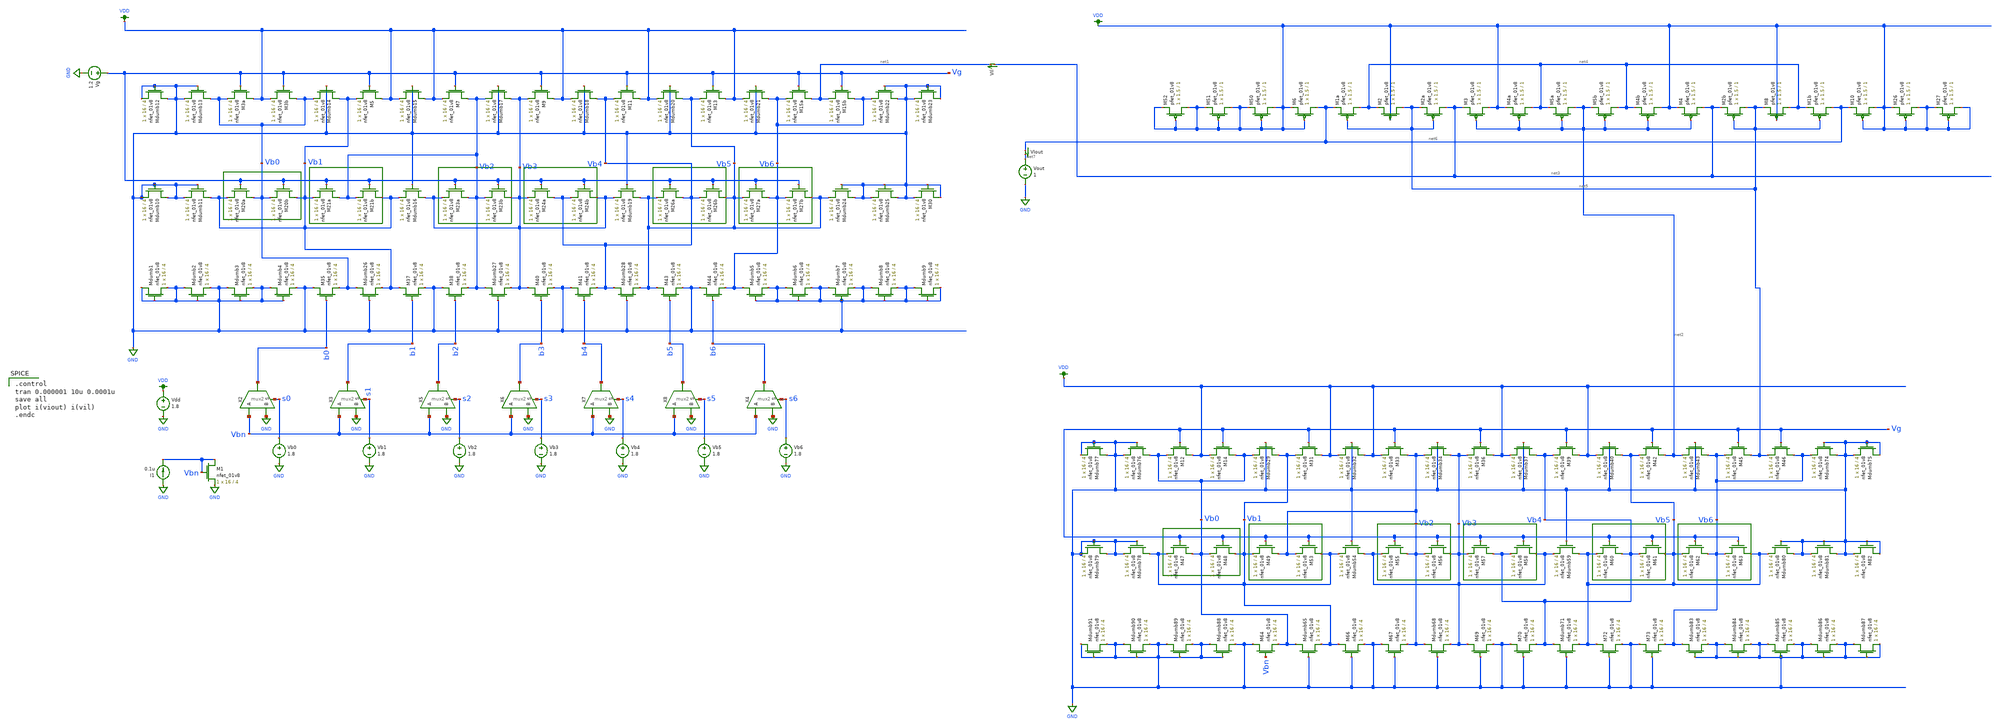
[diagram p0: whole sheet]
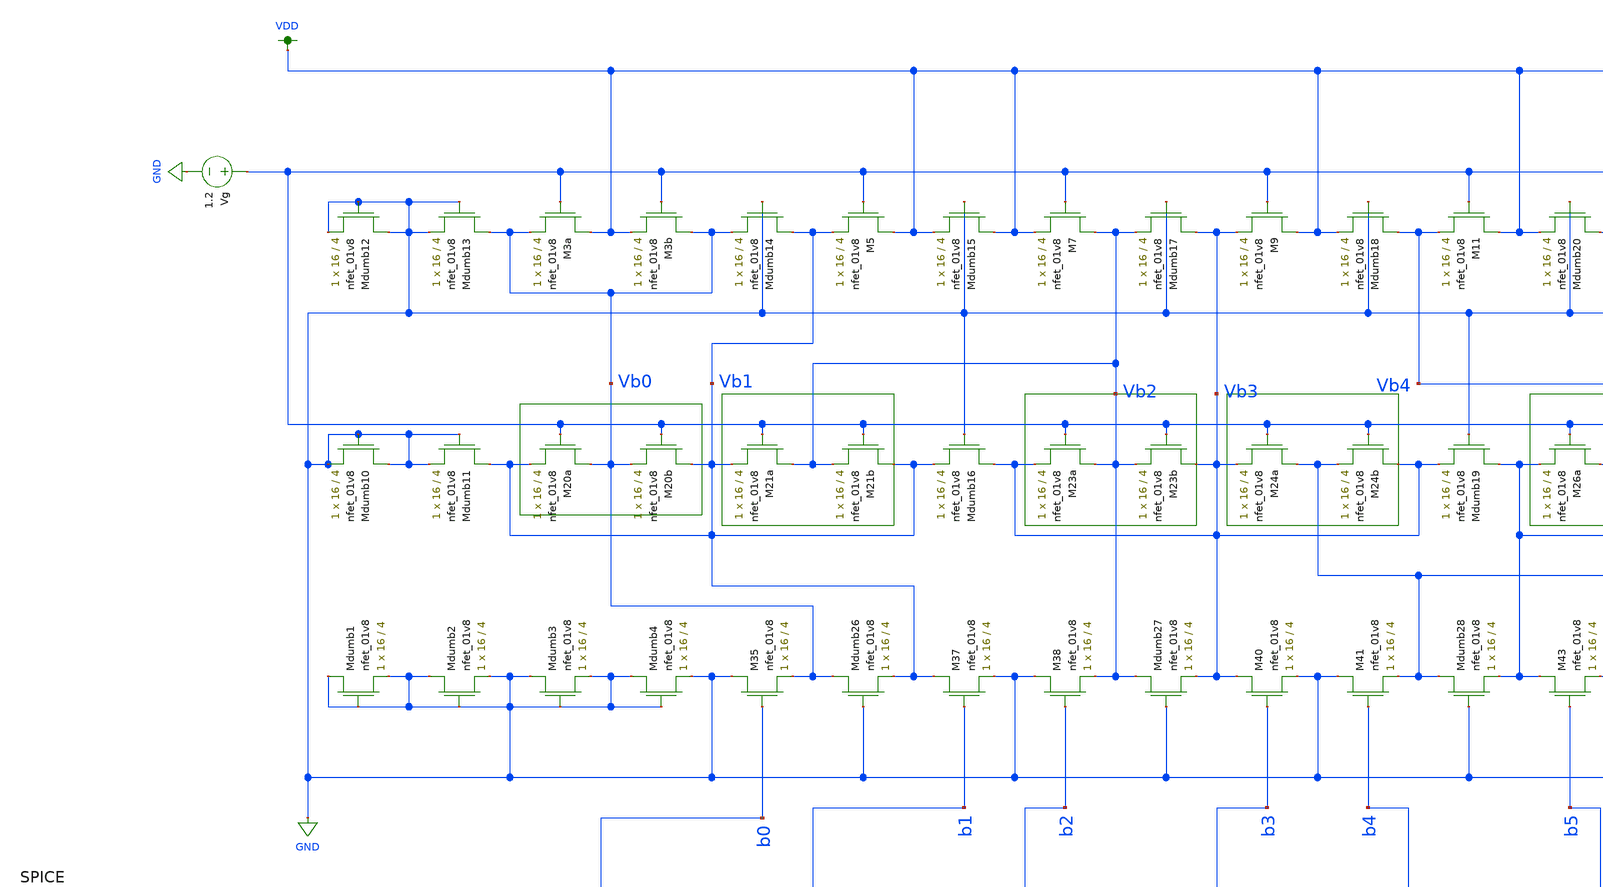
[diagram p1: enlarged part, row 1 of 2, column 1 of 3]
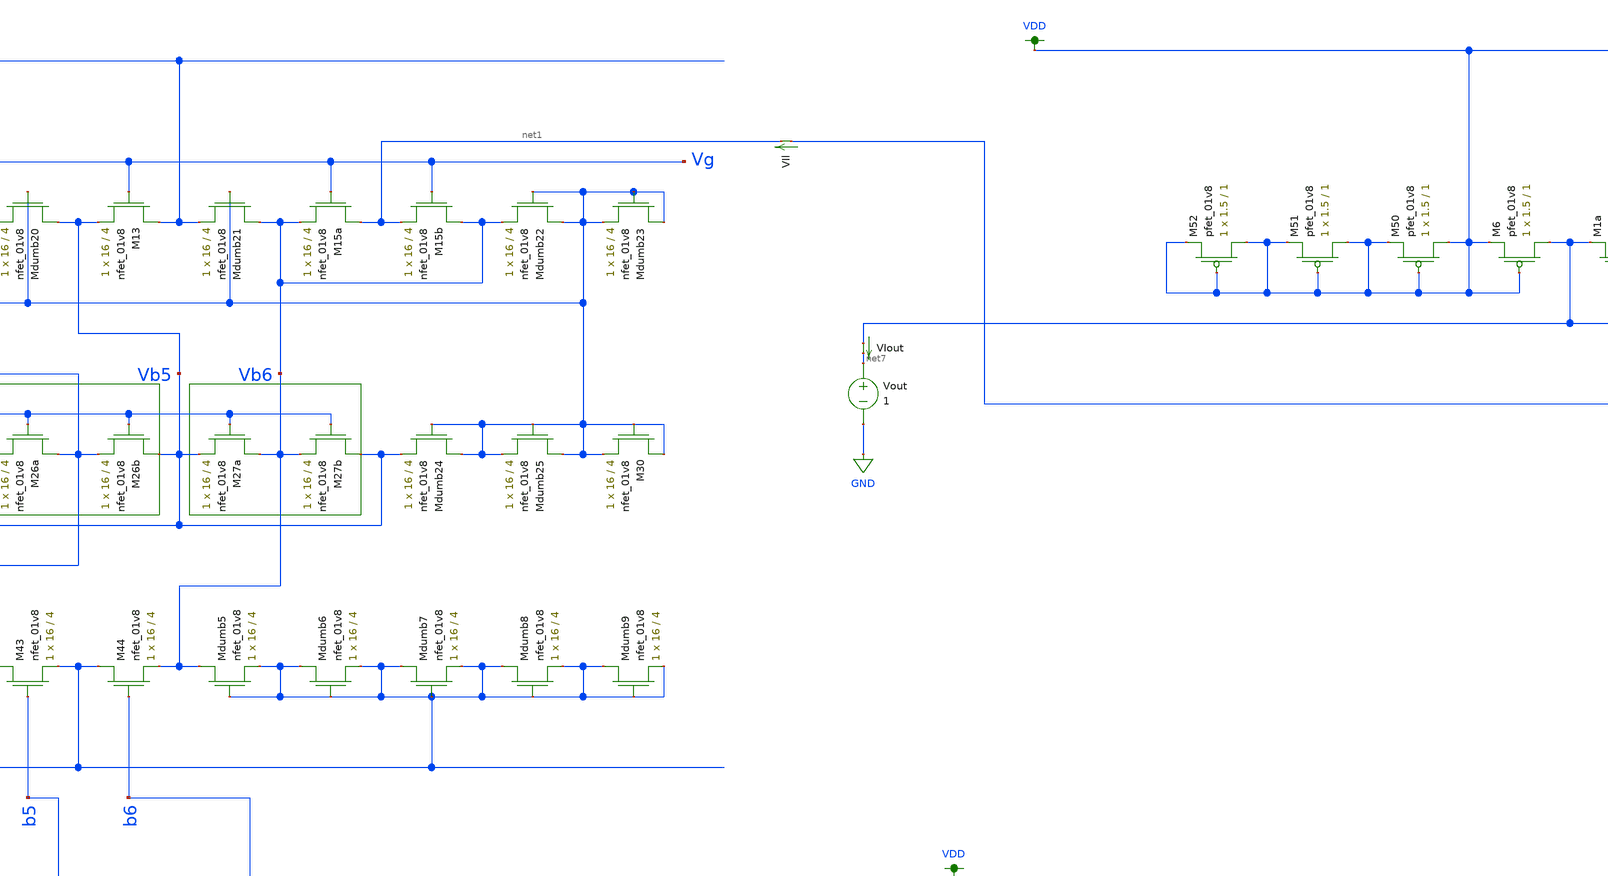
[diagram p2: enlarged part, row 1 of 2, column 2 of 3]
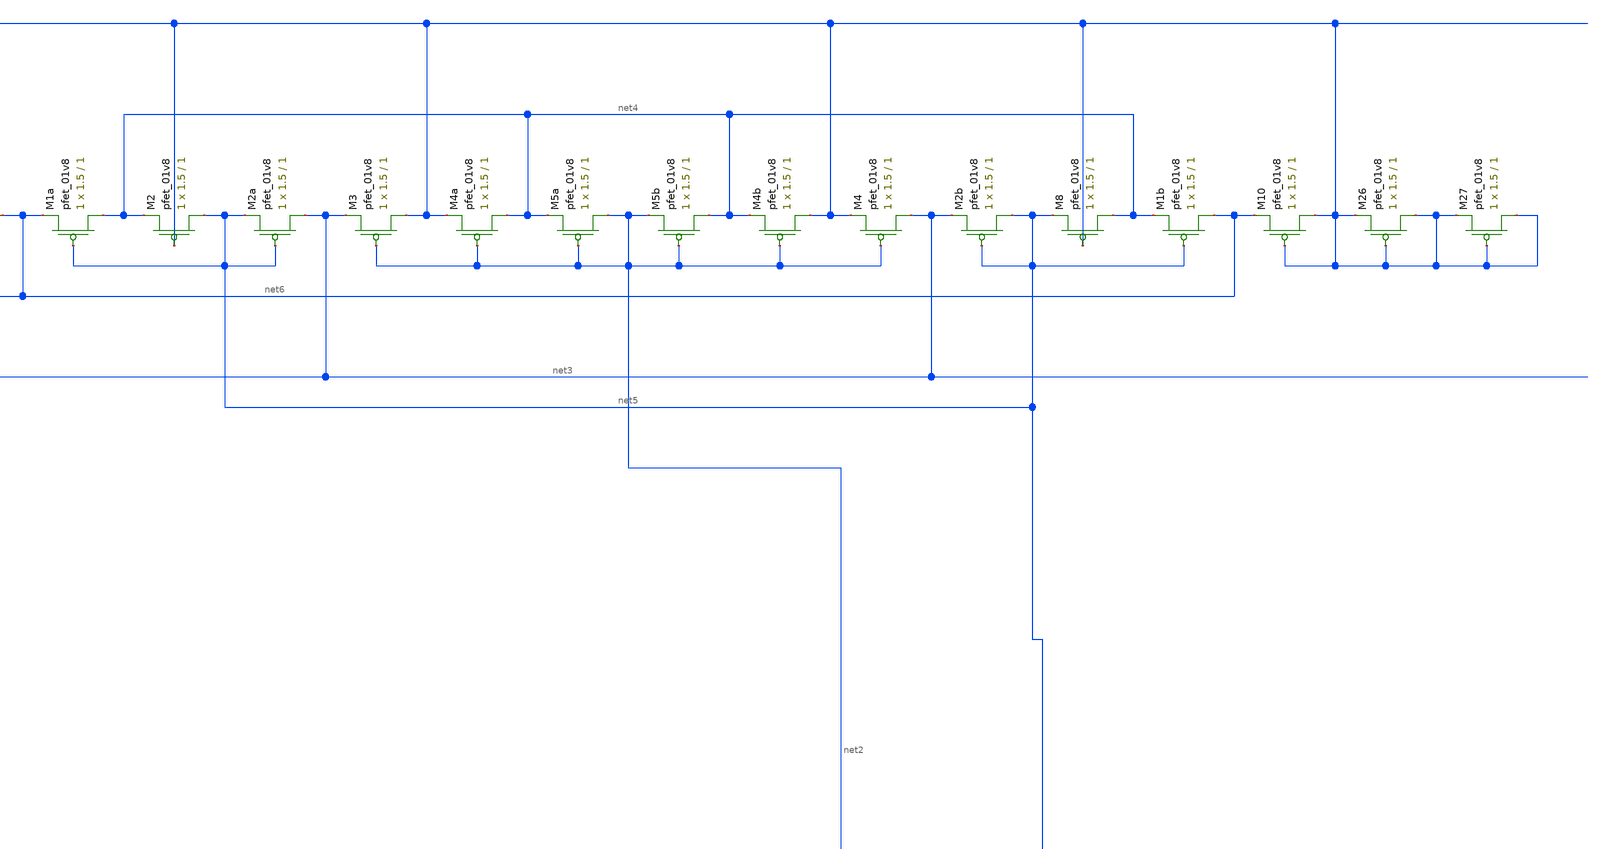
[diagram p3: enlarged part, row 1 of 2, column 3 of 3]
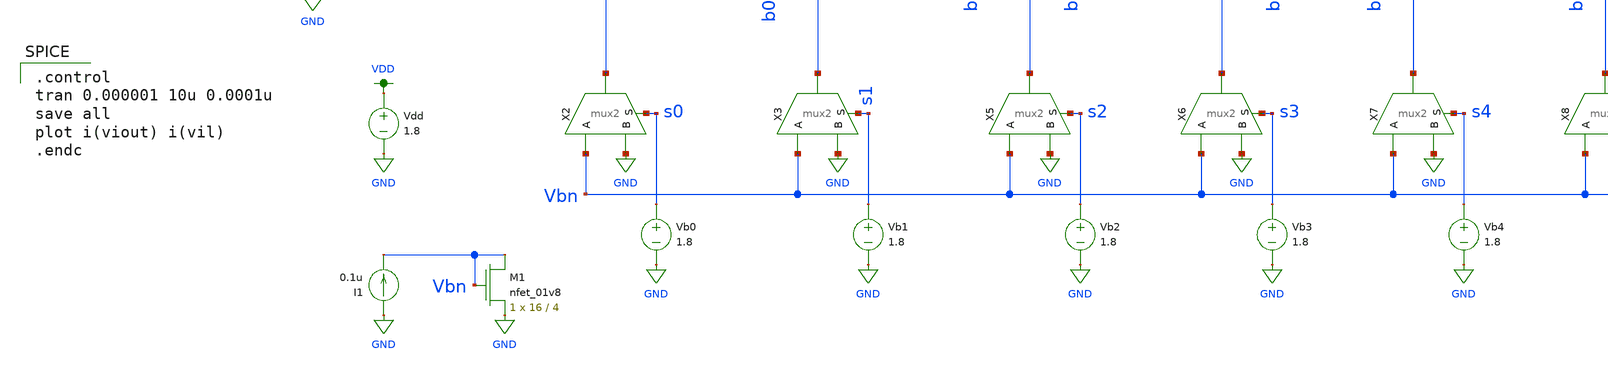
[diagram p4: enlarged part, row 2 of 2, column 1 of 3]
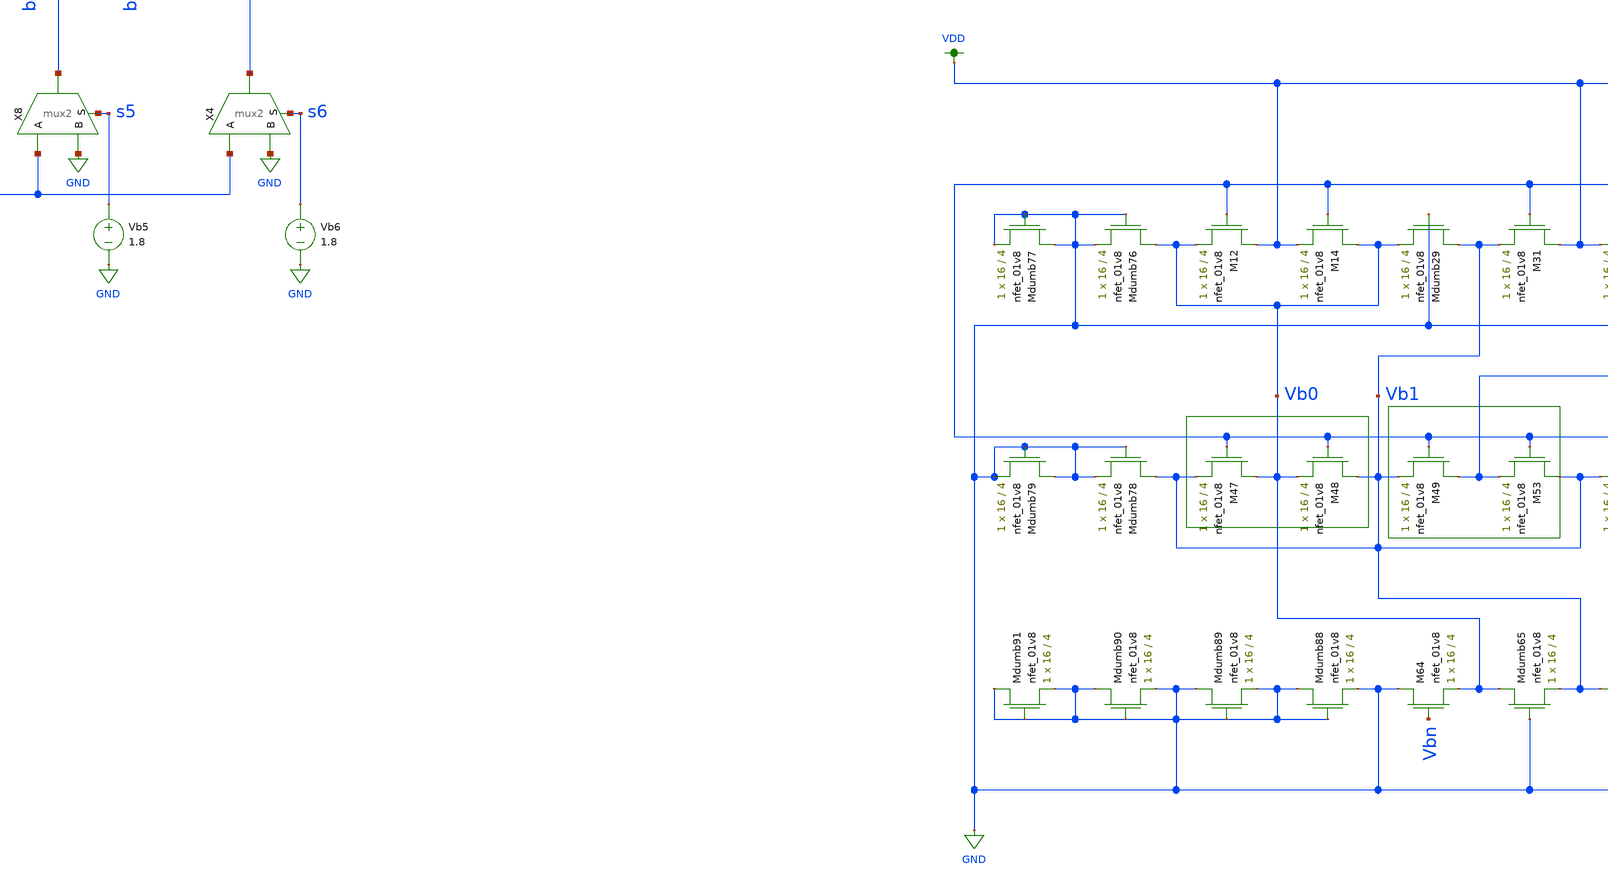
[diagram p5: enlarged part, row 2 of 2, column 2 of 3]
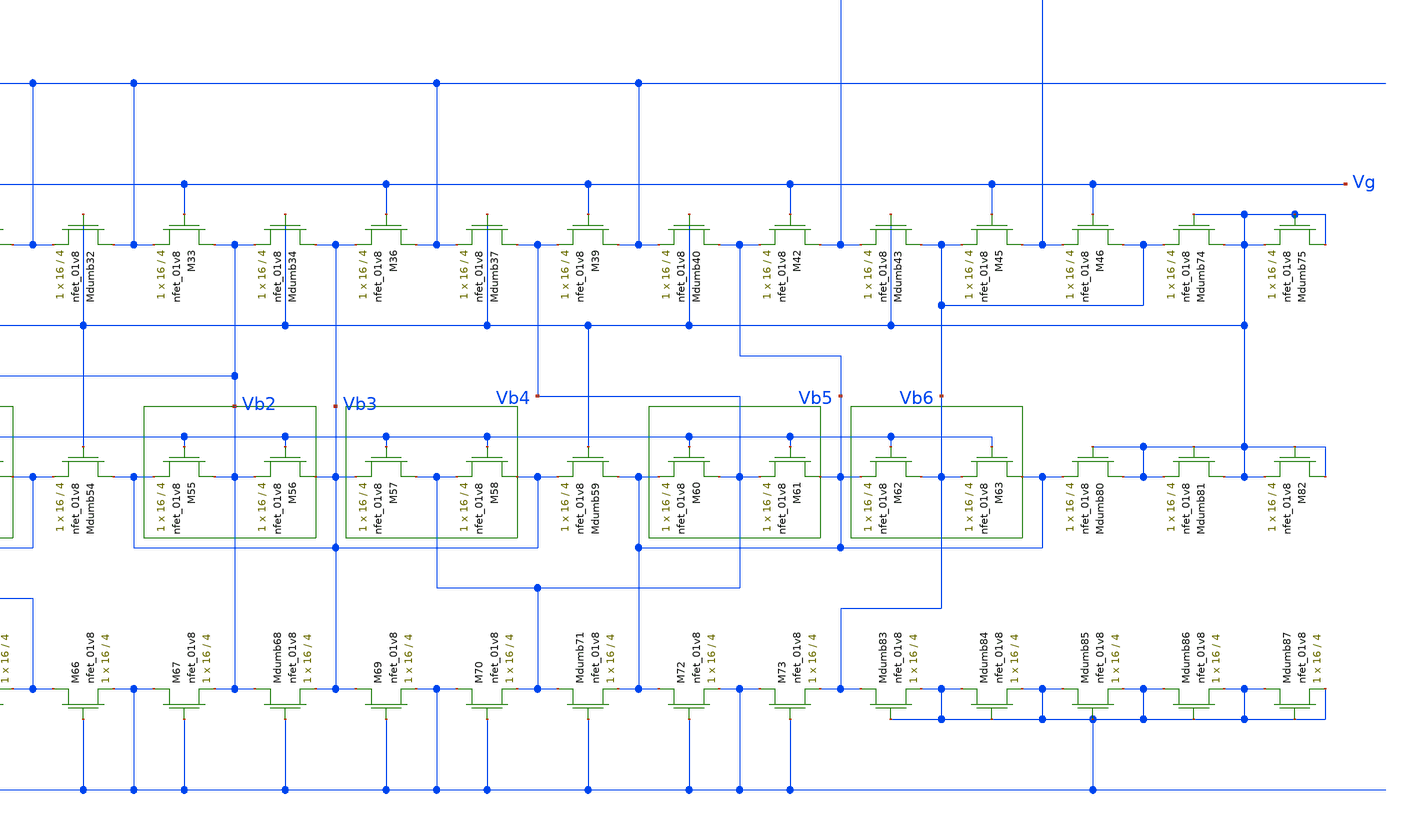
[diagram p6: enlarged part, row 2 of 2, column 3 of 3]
** sch_path: schematic/LDS/test/ladder_test.sch
**.subckt ladder_test
XM3a VDD Vg Vb0 GND sky130_fd_pr__nfet_01v8 L=4 W=16 nf=1 ad='int((nf+1)/2) * W/nf * 0.29' as='int((nf+2)/2) * W/nf * 0.29'
+ pd='2*int((nf+1)/2) * (W/nf + 0.29)' ps='2*int((nf+2)/2) * (W/nf + 0.29)' nrd='0.29 / W' nrs='0.29 / W'
+ sa=0 sb=0 sd=0 mult=1 m=1
XM3b Vb0 Vg VDD GND sky130_fd_pr__nfet_01v8 L=4 W=16 nf=1 ad='int((nf+1)/2) * W/nf * 0.29' as='int((nf+2)/2) * W/nf * 0.29'
+ pd='2*int((nf+1)/2) * (W/nf + 0.29)' ps='2*int((nf+2)/2) * (W/nf + 0.29)' nrd='0.29 / W' nrs='0.29 / W'
+ sa=0 sb=0 sd=0 mult=1 m=1
XMdumb14 Vb1 GND Vb0 GND sky130_fd_pr__nfet_01v8 L=4 W=16 nf=1 ad='int((nf+1)/2) * W/nf * 0.29' as='int((nf+2)/2) * W/nf * 0.29'
+ pd='2*int((nf+1)/2) * (W/nf + 0.29)' ps='2*int((nf+2)/2) * (W/nf + 0.29)' nrd='0.29 / W' nrs='0.29 / W'
+ sa=0 sb=0 sd=0 mult=1 m=1
XM5 VDD Vg Vb1 GND sky130_fd_pr__nfet_01v8 L=4 W=16 nf=1 ad='int((nf+1)/2) * W/nf * 0.29' as='int((nf+2)/2) * W/nf * 0.29'
+ pd='2*int((nf+1)/2) * (W/nf + 0.29)' ps='2*int((nf+2)/2) * (W/nf + 0.29)' nrd='0.29 / W' nrs='0.29 / W'
+ sa=0 sb=0 sd=0 mult=1 m=1
XMdumb15 VDD GND VDD GND sky130_fd_pr__nfet_01v8 L=4 W=16 nf=1 ad='int((nf+1)/2) * W/nf * 0.29' as='int((nf+2)/2) * W/nf * 0.29'
+ pd='2*int((nf+1)/2) * (W/nf + 0.29)' ps='2*int((nf+2)/2) * (W/nf + 0.29)' nrd='0.29 / W' nrs='0.29 / W'
+ sa=0 sb=0 sd=0 mult=1 m=1
XM7 Vb2 Vg VDD GND sky130_fd_pr__nfet_01v8 L=4 W=16 nf=1 ad='int((nf+1)/2) * W/nf * 0.29' as='int((nf+2)/2) * W/nf * 0.29'
+ pd='2*int((nf+1)/2) * (W/nf + 0.29)' ps='2*int((nf+2)/2) * (W/nf + 0.29)' nrd='0.29 / W' nrs='0.29 / W'
+ sa=0 sb=0 sd=0 mult=1 m=1
XMdumb17 Vb3 GND Vb2 GND sky130_fd_pr__nfet_01v8 L=4 W=16 nf=1 ad='int((nf+1)/2) * W/nf * 0.29' as='int((nf+2)/2) * W/nf * 0.29'
+ pd='2*int((nf+1)/2) * (W/nf + 0.29)' ps='2*int((nf+2)/2) * (W/nf + 0.29)' nrd='0.29 / W' nrs='0.29 / W'
+ sa=0 sb=0 sd=0 mult=1 m=1
XM9 VDD Vg Vb3 GND sky130_fd_pr__nfet_01v8 L=4 W=16 nf=1 ad='int((nf+1)/2) * W/nf * 0.29' as='int((nf+2)/2) * W/nf * 0.29'
+ pd='2*int((nf+1)/2) * (W/nf + 0.29)' ps='2*int((nf+2)/2) * (W/nf + 0.29)' nrd='0.29 / W' nrs='0.29 / W'
+ sa=0 sb=0 sd=0 mult=1 m=1
XMdumb18 Vb4 GND VDD GND sky130_fd_pr__nfet_01v8 L=4 W=16 nf=1 ad='int((nf+1)/2) * W/nf * 0.29' as='int((nf+2)/2) * W/nf * 0.29'
+ pd='2*int((nf+1)/2) * (W/nf + 0.29)' ps='2*int((nf+2)/2) * (W/nf + 0.29)' nrd='0.29 / W' nrs='0.29 / W'
+ sa=0 sb=0 sd=0 mult=1 m=1
XM11 VDD Vg Vb4 GND sky130_fd_pr__nfet_01v8 L=4 W=16 nf=1 ad='int((nf+1)/2) * W/nf * 0.29' as='int((nf+2)/2) * W/nf * 0.29'
+ pd='2*int((nf+1)/2) * (W/nf + 0.29)' ps='2*int((nf+2)/2) * (W/nf + 0.29)' nrd='0.29 / W' nrs='0.29 / W'
+ sa=0 sb=0 sd=0 mult=1 m=1
XMdumb20 Vb5 GND VDD GND sky130_fd_pr__nfet_01v8 L=4 W=16 nf=1 ad='int((nf+1)/2) * W/nf * 0.29' as='int((nf+2)/2) * W/nf * 0.29'
+ pd='2*int((nf+1)/2) * (W/nf + 0.29)' ps='2*int((nf+2)/2) * (W/nf + 0.29)' nrd='0.29 / W' nrs='0.29 / W'
+ sa=0 sb=0 sd=0 mult=1 m=1
XM13 VDD Vg Vb5 GND sky130_fd_pr__nfet_01v8 L=4 W=16 nf=1 ad='int((nf+1)/2) * W/nf * 0.29' as='int((nf+2)/2) * W/nf * 0.29'
+ pd='2*int((nf+1)/2) * (W/nf + 0.29)' ps='2*int((nf+2)/2) * (W/nf + 0.29)' nrd='0.29 / W' nrs='0.29 / W'
+ sa=0 sb=0 sd=0 mult=1 m=1
XMdumb21 Vb6 GND VDD GND sky130_fd_pr__nfet_01v8 L=4 W=16 nf=1 ad='int((nf+1)/2) * W/nf * 0.29' as='int((nf+2)/2) * W/nf * 0.29'
+ pd='2*int((nf+1)/2) * (W/nf + 0.29)' ps='2*int((nf+2)/2) * (W/nf + 0.29)' nrd='0.29 / W' nrs='0.29 / W'
+ sa=0 sb=0 sd=0 mult=1 m=1
XM15a net1 Vg Vb6 GND sky130_fd_pr__nfet_01v8 L=4 W=16 nf=1 ad='int((nf+1)/2) * W/nf * 0.29' as='int((nf+2)/2) * W/nf * 0.29'
+ pd='2*int((nf+1)/2) * (W/nf + 0.29)' ps='2*int((nf+2)/2) * (W/nf + 0.29)' nrd='0.29 / W' nrs='0.29 / W'
+ sa=0 sb=0 sd=0 mult=1 m=1
XM15b Vb6 Vg net1 GND sky130_fd_pr__nfet_01v8 L=4 W=16 nf=1 ad='int((nf+1)/2) * W/nf * 0.29' as='int((nf+2)/2) * W/nf * 0.29'
+ pd='2*int((nf+1)/2) * (W/nf + 0.29)' ps='2*int((nf+2)/2) * (W/nf + 0.29)' nrd='0.29 / W' nrs='0.29 / W'
+ sa=0 sb=0 sd=0 mult=1 m=1
XM20a Vb0 Vg Vb1 GND sky130_fd_pr__nfet_01v8 L=4 W=16 nf=1 ad='int((nf+1)/2) * W/nf * 0.29' as='int((nf+2)/2) * W/nf * 0.29'
+ pd='2*int((nf+1)/2) * (W/nf + 0.29)' ps='2*int((nf+2)/2) * (W/nf + 0.29)' nrd='0.29 / W' nrs='0.29 / W'
+ sa=0 sb=0 sd=0 mult=1 m=1
XM20b Vb1 Vg Vb0 GND sky130_fd_pr__nfet_01v8 L=4 W=16 nf=1 ad='int((nf+1)/2) * W/nf * 0.29' as='int((nf+2)/2) * W/nf * 0.29'
+ pd='2*int((nf+1)/2) * (W/nf + 0.29)' ps='2*int((nf+2)/2) * (W/nf + 0.29)' nrd='0.29 / W' nrs='0.29 / W'
+ sa=0 sb=0 sd=0 mult=1 m=1
XM21a Vb2 Vg Vb1 GND sky130_fd_pr__nfet_01v8 L=4 W=16 nf=1 ad='int((nf+1)/2) * W/nf * 0.29' as='int((nf+2)/2) * W/nf * 0.29'
+ pd='2*int((nf+1)/2) * (W/nf + 0.29)' ps='2*int((nf+2)/2) * (W/nf + 0.29)' nrd='0.29 / W' nrs='0.29 / W'
+ sa=0 sb=0 sd=0 mult=1 m=1
XM21b Vb1 Vg Vb2 GND sky130_fd_pr__nfet_01v8 L=4 W=16 nf=1 ad='int((nf+1)/2) * W/nf * 0.29' as='int((nf+2)/2) * W/nf * 0.29'
+ pd='2*int((nf+1)/2) * (W/nf + 0.29)' ps='2*int((nf+2)/2) * (W/nf + 0.29)' nrd='0.29 / W' nrs='0.29 / W'
+ sa=0 sb=0 sd=0 mult=1 m=1
XMdumb16 Vb3 GND Vb1 GND sky130_fd_pr__nfet_01v8 L=4 W=16 nf=1 ad='int((nf+1)/2) * W/nf * 0.29' as='int((nf+2)/2) * W/nf * 0.29'
+ pd='2*int((nf+1)/2) * (W/nf + 0.29)' ps='2*int((nf+2)/2) * (W/nf + 0.29)' nrd='0.29 / W' nrs='0.29 / W'
+ sa=0 sb=0 sd=0 mult=1 m=1
XM23a Vb2 Vg Vb3 GND sky130_fd_pr__nfet_01v8 L=4 W=16 nf=1 ad='int((nf+1)/2) * W/nf * 0.29' as='int((nf+2)/2) * W/nf * 0.29'
+ pd='2*int((nf+1)/2) * (W/nf + 0.29)' ps='2*int((nf+2)/2) * (W/nf + 0.29)' nrd='0.29 / W' nrs='0.29 / W'
+ sa=0 sb=0 sd=0 mult=1 m=1
XM23b Vb3 Vg Vb2 GND sky130_fd_pr__nfet_01v8 L=4 W=16 nf=1 ad='int((nf+1)/2) * W/nf * 0.29' as='int((nf+2)/2) * W/nf * 0.29'
+ pd='2*int((nf+1)/2) * (W/nf + 0.29)' ps='2*int((nf+2)/2) * (W/nf + 0.29)' nrd='0.29 / W' nrs='0.29 / W'
+ sa=0 sb=0 sd=0 mult=1 m=1
XM24a Vb4 Vg Vb3 GND sky130_fd_pr__nfet_01v8 L=4 W=16 nf=1 ad='int((nf+1)/2) * W/nf * 0.29' as='int((nf+2)/2) * W/nf * 0.29'
+ pd='2*int((nf+1)/2) * (W/nf + 0.29)' ps='2*int((nf+2)/2) * (W/nf + 0.29)' nrd='0.29 / W' nrs='0.29 / W'
+ sa=0 sb=0 sd=0 mult=1 m=1
XM24b Vb3 Vg Vb4 GND sky130_fd_pr__nfet_01v8 L=4 W=16 nf=1 ad='int((nf+1)/2) * W/nf * 0.29' as='int((nf+2)/2) * W/nf * 0.29'
+ pd='2*int((nf+1)/2) * (W/nf + 0.29)' ps='2*int((nf+2)/2) * (W/nf + 0.29)' nrd='0.29 / W' nrs='0.29 / W'
+ sa=0 sb=0 sd=0 mult=1 m=1
XMdumb19 Vb5 GND Vb3 GND sky130_fd_pr__nfet_01v8 L=4 W=16 nf=1 ad='int((nf+1)/2) * W/nf * 0.29' as='int((nf+2)/2) * W/nf * 0.29'
+ pd='2*int((nf+1)/2) * (W/nf + 0.29)' ps='2*int((nf+2)/2) * (W/nf + 0.29)' nrd='0.29 / W' nrs='0.29 / W'
+ sa=0 sb=0 sd=0 mult=1 m=1
XM26a Vb4 Vg Vb5 GND sky130_fd_pr__nfet_01v8 L=4 W=16 nf=1 ad='int((nf+1)/2) * W/nf * 0.29' as='int((nf+2)/2) * W/nf * 0.29'
+ pd='2*int((nf+1)/2) * (W/nf + 0.29)' ps='2*int((nf+2)/2) * (W/nf + 0.29)' nrd='0.29 / W' nrs='0.29 / W'
+ sa=0 sb=0 sd=0 mult=1 m=1
XM26b Vb5 Vg Vb4 GND sky130_fd_pr__nfet_01v8 L=4 W=16 nf=1 ad='int((nf+1)/2) * W/nf * 0.29' as='int((nf+2)/2) * W/nf * 0.29'
+ pd='2*int((nf+1)/2) * (W/nf + 0.29)' ps='2*int((nf+2)/2) * (W/nf + 0.29)' nrd='0.29 / W' nrs='0.29 / W'
+ sa=0 sb=0 sd=0 mult=1 m=1
XM27a Vb6 Vg Vb5 GND sky130_fd_pr__nfet_01v8 L=4 W=16 nf=1 ad='int((nf+1)/2) * W/nf * 0.29' as='int((nf+2)/2) * W/nf * 0.29'
+ pd='2*int((nf+1)/2) * (W/nf + 0.29)' ps='2*int((nf+2)/2) * (W/nf + 0.29)' nrd='0.29 / W' nrs='0.29 / W'
+ sa=0 sb=0 sd=0 mult=1 m=1
XM27b Vb5 Vg Vb6 GND sky130_fd_pr__nfet_01v8 L=4 W=16 nf=1 ad='int((nf+1)/2) * W/nf * 0.29' as='int((nf+2)/2) * W/nf * 0.29'
+ pd='2*int((nf+1)/2) * (W/nf + 0.29)' ps='2*int((nf+2)/2) * (W/nf + 0.29)' nrd='0.29 / W' nrs='0.29 / W'
+ sa=0 sb=0 sd=0 mult=1 m=1
XM35 GND b0 Vb0 GND sky130_fd_pr__nfet_01v8 L=4 W=16 nf=1 ad='int((nf+1)/2) * W/nf * 0.29' as='int((nf+2)/2) * W/nf * 0.29'
+ pd='2*int((nf+1)/2) * (W/nf + 0.29)' ps='2*int((nf+2)/2) * (W/nf + 0.29)' nrd='0.29 / W' nrs='0.29 / W'
+ sa=0 sb=0 sd=0 mult=1 m=1
XMdumb26 Vb0 GND Vb1 GND sky130_fd_pr__nfet_01v8 L=4 W=16 nf=1 ad='int((nf+1)/2) * W/nf * 0.29' as='int((nf+2)/2) * W/nf * 0.29'
+ pd='2*int((nf+1)/2) * (W/nf + 0.29)' ps='2*int((nf+2)/2) * (W/nf + 0.29)' nrd='0.29 / W' nrs='0.29 / W'
+ sa=0 sb=0 sd=0 mult=1 m=1
XM37 Vb1 b1 GND GND sky130_fd_pr__nfet_01v8 L=4 W=16 nf=1 ad='int((nf+1)/2) * W/nf * 0.29' as='int((nf+2)/2) * W/nf * 0.29'
+ pd='2*int((nf+1)/2) * (W/nf + 0.29)' ps='2*int((nf+2)/2) * (W/nf + 0.29)' nrd='0.29 / W' nrs='0.29 / W'
+ sa=0 sb=0 sd=0 mult=1 m=1
XM38 GND b2 Vb2 GND sky130_fd_pr__nfet_01v8 L=4 W=16 nf=1 ad='int((nf+1)/2) * W/nf * 0.29' as='int((nf+2)/2) * W/nf * 0.29'
+ pd='2*int((nf+1)/2) * (W/nf + 0.29)' ps='2*int((nf+2)/2) * (W/nf + 0.29)' nrd='0.29 / W' nrs='0.29 / W'
+ sa=0 sb=0 sd=0 mult=1 m=1
XMdumb27 Vb2 GND Vb3 GND sky130_fd_pr__nfet_01v8 L=4 W=16 nf=1 ad='int((nf+1)/2) * W/nf * 0.29' as='int((nf+2)/2) * W/nf * 0.29'
+ pd='2*int((nf+1)/2) * (W/nf + 0.29)' ps='2*int((nf+2)/2) * (W/nf + 0.29)' nrd='0.29 / W' nrs='0.29 / W'
+ sa=0 sb=0 sd=0 mult=1 m=1
XM40 Vb3 b3 GND GND sky130_fd_pr__nfet_01v8 L=4 W=16 nf=1 ad='int((nf+1)/2) * W/nf * 0.29' as='int((nf+2)/2) * W/nf * 0.29'
+ pd='2*int((nf+1)/2) * (W/nf + 0.29)' ps='2*int((nf+2)/2) * (W/nf + 0.29)' nrd='0.29 / W' nrs='0.29 / W'
+ sa=0 sb=0 sd=0 mult=1 m=1
XM41 GND b4 Vb4 GND sky130_fd_pr__nfet_01v8 L=4 W=16 nf=1 ad='int((nf+1)/2) * W/nf * 0.29' as='int((nf+2)/2) * W/nf * 0.29'
+ pd='2*int((nf+1)/2) * (W/nf + 0.29)' ps='2*int((nf+2)/2) * (W/nf + 0.29)' nrd='0.29 / W' nrs='0.29 / W'
+ sa=0 sb=0 sd=0 mult=1 m=1
XMdumb28 Vb4 GND Vb5 GND sky130_fd_pr__nfet_01v8 L=4 W=16 nf=1 ad='int((nf+1)/2) * W/nf * 0.29' as='int((nf+2)/2) * W/nf * 0.29'
+ pd='2*int((nf+1)/2) * (W/nf + 0.29)' ps='2*int((nf+2)/2) * (W/nf + 0.29)' nrd='0.29 / W' nrs='0.29 / W'
+ sa=0 sb=0 sd=0 mult=1 m=1
XM43 Vb5 b5 GND GND sky130_fd_pr__nfet_01v8 L=4 W=16 nf=1 ad='int((nf+1)/2) * W/nf * 0.29' as='int((nf+2)/2) * W/nf * 0.29'
+ pd='2*int((nf+1)/2) * (W/nf + 0.29)' ps='2*int((nf+2)/2) * (W/nf + 0.29)' nrd='0.29 / W' nrs='0.29 / W'
+ sa=0 sb=0 sd=0 mult=1 m=1
XM44 GND b6 Vb6 GND sky130_fd_pr__nfet_01v8 L=4 W=16 nf=1 ad='int((nf+1)/2) * W/nf * 0.29' as='int((nf+2)/2) * W/nf * 0.29'
+ pd='2*int((nf+1)/2) * (W/nf + 0.29)' ps='2*int((nf+2)/2) * (W/nf + 0.29)' nrd='0.29 / W' nrs='0.29 / W'
+ sa=0 sb=0 sd=0 mult=1 m=1
XMdumb22 GND GND Vb6 GND sky130_fd_pr__nfet_01v8 L=4 W=16 nf=1 ad='int((nf+1)/2) * W/nf * 0.29' as='int((nf+2)/2) * W/nf * 0.29'
+ pd='2*int((nf+1)/2) * (W/nf + 0.29)' ps='2*int((nf+2)/2) * (W/nf + 0.29)' nrd='0.29 / W' nrs='0.29 / W'
+ sa=0 sb=0 sd=0 mult=1 m=1
XMdumb23 GND GND GND GND sky130_fd_pr__nfet_01v8 L=4 W=16 nf=1 ad='int((nf+1)/2) * W/nf * 0.29' as='int((nf+2)/2) * W/nf * 0.29'
+ pd='2*int((nf+1)/2) * (W/nf + 0.29)' ps='2*int((nf+2)/2) * (W/nf + 0.29)' nrd='0.29 / W' nrs='0.29 / W'
+ sa=0 sb=0 sd=0 mult=1 m=1
XMdumb13 Vb0 GND GND GND sky130_fd_pr__nfet_01v8 L=4 W=16 nf=1 ad='int((nf+1)/2) * W/nf * 0.29' as='int((nf+2)/2) * W/nf * 0.29'
+ pd='2*int((nf+1)/2) * (W/nf + 0.29)' ps='2*int((nf+2)/2) * (W/nf + 0.29)' nrd='0.29 / W' nrs='0.29 / W'
+ sa=0 sb=0 sd=0 mult=1 m=1
XMdumb12 GND GND GND GND sky130_fd_pr__nfet_01v8 L=4 W=16 nf=1 ad='int((nf+1)/2) * W/nf * 0.29' as='int((nf+2)/2) * W/nf * 0.29'
+ pd='2*int((nf+1)/2) * (W/nf + 0.29)' ps='2*int((nf+2)/2) * (W/nf + 0.29)' nrd='0.29 / W' nrs='0.29 / W'
+ sa=0 sb=0 sd=0 mult=1 m=1
XMdumb11 Vb1 GND GND GND sky130_fd_pr__nfet_01v8 L=4 W=16 nf=1 ad='int((nf+1)/2) * W/nf * 0.29' as='int((nf+2)/2) * W/nf * 0.29'
+ pd='2*int((nf+1)/2) * (W/nf + 0.29)' ps='2*int((nf+2)/2) * (W/nf + 0.29)' nrd='0.29 / W' nrs='0.29 / W'
+ sa=0 sb=0 sd=0 mult=1 m=1
XMdumb10 GND GND GND GND sky130_fd_pr__nfet_01v8 L=4 W=16 nf=1 ad='int((nf+1)/2) * W/nf * 0.29' as='int((nf+2)/2) * W/nf * 0.29'
+ pd='2*int((nf+1)/2) * (W/nf + 0.29)' ps='2*int((nf+2)/2) * (W/nf + 0.29)' nrd='0.29 / W' nrs='0.29 / W'
+ sa=0 sb=0 sd=0 mult=1 m=1
XMdumb24 GND GND Vb5 GND sky130_fd_pr__nfet_01v8 L=4 W=16 nf=1 ad='int((nf+1)/2) * W/nf * 0.29' as='int((nf+2)/2) * W/nf * 0.29'
+ pd='2*int((nf+1)/2) * (W/nf + 0.29)' ps='2*int((nf+2)/2) * (W/nf + 0.29)' nrd='0.29 / W' nrs='0.29 / W'
+ sa=0 sb=0 sd=0 mult=1 m=1
XMdumb25 GND GND GND GND sky130_fd_pr__nfet_01v8 L=4 W=16 nf=1 ad='int((nf+1)/2) * W/nf * 0.29' as='int((nf+2)/2) * W/nf * 0.29'
+ pd='2*int((nf+1)/2) * (W/nf + 0.29)' ps='2*int((nf+2)/2) * (W/nf + 0.29)' nrd='0.29 / W' nrs='0.29 / W'
+ sa=0 sb=0 sd=0 mult=1 m=1
XM30 GND GND GND GND sky130_fd_pr__nfet_01v8 L=4 W=16 nf=1 ad='int((nf+1)/2) * W/nf * 0.29' as='int((nf+2)/2) * W/nf * 0.29'
+ pd='2*int((nf+1)/2) * (W/nf + 0.29)' ps='2*int((nf+2)/2) * (W/nf + 0.29)' nrd='0.29 / W' nrs='0.29 / W'
+ sa=0 sb=0 sd=0 mult=1 m=1
XMdumb5 Vb6 GND GND GND sky130_fd_pr__nfet_01v8 L=4 W=16 nf=1 ad='int((nf+1)/2) * W/nf * 0.29' as='int((nf+2)/2) * W/nf * 0.29'
+ pd='2*int((nf+1)/2) * (W/nf + 0.29)' ps='2*int((nf+2)/2) * (W/nf + 0.29)' nrd='0.29 / W' nrs='0.29 / W'
+ sa=0 sb=0 sd=0 mult=1 m=1
XMdumb6 GND GND GND GND sky130_fd_pr__nfet_01v8 L=4 W=16 nf=1 ad='int((nf+1)/2) * W/nf * 0.29' as='int((nf+2)/2) * W/nf * 0.29'
+ pd='2*int((nf+1)/2) * (W/nf + 0.29)' ps='2*int((nf+2)/2) * (W/nf + 0.29)' nrd='0.29 / W' nrs='0.29 / W'
+ sa=0 sb=0 sd=0 mult=1 m=1
XMdumb7 GND GND GND GND sky130_fd_pr__nfet_01v8 L=4 W=16 nf=1 ad='int((nf+1)/2) * W/nf * 0.29' as='int((nf+2)/2) * W/nf * 0.29'
+ pd='2*int((nf+1)/2) * (W/nf + 0.29)' ps='2*int((nf+2)/2) * (W/nf + 0.29)' nrd='0.29 / W' nrs='0.29 / W'
+ sa=0 sb=0 sd=0 mult=1 m=1
XMdumb8 GND GND GND GND sky130_fd_pr__nfet_01v8 L=4 W=16 nf=1 ad='int((nf+1)/2) * W/nf * 0.29' as='int((nf+2)/2) * W/nf * 0.29'
+ pd='2*int((nf+1)/2) * (W/nf + 0.29)' ps='2*int((nf+2)/2) * (W/nf + 0.29)' nrd='0.29 / W' nrs='0.29 / W'
+ sa=0 sb=0 sd=0 mult=1 m=1
XMdumb9 GND GND GND GND sky130_fd_pr__nfet_01v8 L=4 W=16 nf=1 ad='int((nf+1)/2) * W/nf * 0.29' as='int((nf+2)/2) * W/nf * 0.29'
+ pd='2*int((nf+1)/2) * (W/nf + 0.29)' ps='2*int((nf+2)/2) * (W/nf + 0.29)' nrd='0.29 / W' nrs='0.29 / W'
+ sa=0 sb=0 sd=0 mult=1 m=1
XMdumb4 GND GND GND GND sky130_fd_pr__nfet_01v8 L=4 W=16 nf=1 ad='int((nf+1)/2) * W/nf * 0.29' as='int((nf+2)/2) * W/nf * 0.29'
+ pd='2*int((nf+1)/2) * (W/nf + 0.29)' ps='2*int((nf+2)/2) * (W/nf + 0.29)' nrd='0.29 / W' nrs='0.29 / W'
+ sa=0 sb=0 sd=0 mult=1 m=1
XMdumb3 GND GND GND GND sky130_fd_pr__nfet_01v8 L=4 W=16 nf=1 ad='int((nf+1)/2) * W/nf * 0.29' as='int((nf+2)/2) * W/nf * 0.29'
+ pd='2*int((nf+1)/2) * (W/nf + 0.29)' ps='2*int((nf+2)/2) * (W/nf + 0.29)' nrd='0.29 / W' nrs='0.29 / W'
+ sa=0 sb=0 sd=0 mult=1 m=1
XMdumb2 GND GND GND GND sky130_fd_pr__nfet_01v8 L=4 W=16 nf=1 ad='int((nf+1)/2) * W/nf * 0.29' as='int((nf+2)/2) * W/nf * 0.29'
+ pd='2*int((nf+1)/2) * (W/nf + 0.29)' ps='2*int((nf+2)/2) * (W/nf + 0.29)' nrd='0.29 / W' nrs='0.29 / W'
+ sa=0 sb=0 sd=0 mult=1 m=1
XMdumb1 GND GND GND GND sky130_fd_pr__nfet_01v8 L=4 W=16 nf=1 ad='int((nf+1)/2) * W/nf * 0.29' as='int((nf+2)/2) * W/nf * 0.29'
+ pd='2*int((nf+1)/2) * (W/nf + 0.29)' ps='2*int((nf+2)/2) * (W/nf + 0.29)' nrd='0.29 / W' nrs='0.29 / W'
+ sa=0 sb=0 sd=0 mult=1 m=1
Vg Vg GND 1.2
Vdd VDD GND 1.8
I1 GND Vbn 0.1u
X2 b0 Vbn GND s0 mux2
X3 b1 Vbn GND s1 mux2
Vb0 s0 GND 1.8
Vb1 s1 GND 1.8
Vb2 s2 GND 1.8
X5 b2 Vbn GND s2 mux2
Vb3 s3 GND 1.8
X6 b3 Vbn GND s3 mux2
Vb4 s4 GND 1.8
X7 b4 Vbn GND s4 mux2
Vb5 s5 GND 1.8
X8 b5 Vbn GND s5 mux2
Vb6 s6 GND 1.8
X4 b6 Vbn GND s6 mux2
XM1 Vbn Vbn GND GND sky130_fd_pr__nfet_01v8 L=4 W=16 nf=1 ad='int((nf+1)/2) * W/nf * 0.29' as='int((nf+2)/2) * W/nf * 0.29'
+ pd='2*int((nf+1)/2) * (W/nf + 0.29)' ps='2*int((nf+2)/2) * (W/nf + 0.29)' nrd='0.29 / W' nrs='0.29 / W'
+ sa=0 sb=0 sd=0 mult=1 m=1
XM2 net5 VDD net4 VDD sky130_fd_pr__pfet_01v8 L=1 W=1.5 nf=1 ad='int((nf+1)/2) * W/nf * 0.29' as='int((nf+2)/2) * W/nf * 0.29'
+ pd='2*int((nf+1)/2) * (W/nf + 0.29)' ps='2*int((nf+2)/2) * (W/nf + 0.29)' nrd='0.29 / W' nrs='0.29 / W'
+ sa=0 sb=0 sd=0 mult=1 m=1
XM2a net3 net5 net5 VDD sky130_fd_pr__pfet_01v8 L=1 W=1.5 nf=1 ad='int((nf+1)/2) * W/nf * 0.29' as='int((nf+2)/2) * W/nf * 0.29'
+ pd='2*int((nf+1)/2) * (W/nf + 0.29)' ps='2*int((nf+2)/2) * (W/nf + 0.29)' nrd='0.29 / W' nrs='0.29 / W'
+ sa=0 sb=0 sd=0 mult=1 m=1
XM3 VDD net2 net3 VDD sky130_fd_pr__pfet_01v8 L=1 W=1.5 nf=1 ad='int((nf+1)/2) * W/nf * 0.29' as='int((nf+2)/2) * W/nf * 0.29'
+ pd='2*int((nf+1)/2) * (W/nf + 0.29)' ps='2*int((nf+2)/2) * (W/nf + 0.29)' nrd='0.29 / W' nrs='0.29 / W'
+ sa=0 sb=0 sd=0 mult=1 m=1
XM4a net4 net2 VDD VDD sky130_fd_pr__pfet_01v8 L=1 W=1.5 nf=1 ad='int((nf+1)/2) * W/nf * 0.29' as='int((nf+2)/2) * W/nf * 0.29'
+ pd='2*int((nf+1)/2) * (W/nf + 0.29)' ps='2*int((nf+2)/2) * (W/nf + 0.29)' nrd='0.29 / W' nrs='0.29 / W'
+ sa=0 sb=0 sd=0 mult=1 m=1
XM5a net2 net2 net4 VDD sky130_fd_pr__pfet_01v8 L=1 W=1.5 nf=1 ad='int((nf+1)/2) * W/nf * 0.29' as='int((nf+2)/2) * W/nf * 0.29'
+ pd='2*int((nf+1)/2) * (W/nf + 0.29)' ps='2*int((nf+2)/2) * (W/nf + 0.29)' nrd='0.29 / W' nrs='0.29 / W'
+ sa=0 sb=0 sd=0 mult=1 m=1
XM5b net4 net2 net2 VDD sky130_fd_pr__pfet_01v8 L=1 W=1.5 nf=1 ad='int((nf+1)/2) * W/nf * 0.29' as='int((nf+2)/2) * W/nf * 0.29'
+ pd='2*int((nf+1)/2) * (W/nf + 0.29)' ps='2*int((nf+2)/2) * (W/nf + 0.29)' nrd='0.29 / W' nrs='0.29 / W'
+ sa=0 sb=0 sd=0 mult=1 m=1
XM4b VDD net2 net4 VDD sky130_fd_pr__pfet_01v8 L=1 W=1.5 nf=1 ad='int((nf+1)/2) * W/nf * 0.29' as='int((nf+2)/2) * W/nf * 0.29'
+ pd='2*int((nf+1)/2) * (W/nf + 0.29)' ps='2*int((nf+2)/2) * (W/nf + 0.29)' nrd='0.29 / W' nrs='0.29 / W'
+ sa=0 sb=0 sd=0 mult=1 m=1
XM4 net3 net2 VDD VDD sky130_fd_pr__pfet_01v8 L=1 W=1.5 nf=1 ad='int((nf+1)/2) * W/nf * 0.29' as='int((nf+2)/2) * W/nf * 0.29'
+ pd='2*int((nf+1)/2) * (W/nf + 0.29)' ps='2*int((nf+2)/2) * (W/nf + 0.29)' nrd='0.29 / W' nrs='0.29 / W'
+ sa=0 sb=0 sd=0 mult=1 m=1
XM2b net5 net5 net3 VDD sky130_fd_pr__pfet_01v8 L=1 W=1.5 nf=1 ad='int((nf+1)/2) * W/nf * 0.29' as='int((nf+2)/2) * W/nf * 0.29'
+ pd='2*int((nf+1)/2) * (W/nf + 0.29)' ps='2*int((nf+2)/2) * (W/nf + 0.29)' nrd='0.29 / W' nrs='0.29 / W'
+ sa=0 sb=0 sd=0 mult=1 m=1
XM8 net4 VDD net5 VDD sky130_fd_pr__pfet_01v8 L=1 W=1.5 nf=1 ad='int((nf+1)/2) * W/nf * 0.29' as='int((nf+2)/2) * W/nf * 0.29'
+ pd='2*int((nf+1)/2) * (W/nf + 0.29)' ps='2*int((nf+2)/2) * (W/nf + 0.29)' nrd='0.29 / W' nrs='0.29 / W'
+ sa=0 sb=0 sd=0 mult=1 m=1
XM1a net4 net5 net6 VDD sky130_fd_pr__pfet_01v8 L=1 W=1.5 nf=1 ad='int((nf+1)/2) * W/nf * 0.29' as='int((nf+2)/2) * W/nf * 0.29'
+ pd='2*int((nf+1)/2) * (W/nf + 0.29)' ps='2*int((nf+2)/2) * (W/nf + 0.29)' nrd='0.29 / W' nrs='0.29 / W'
+ sa=0 sb=0 sd=0 mult=1 m=1
XM1b net6 net5 net4 VDD sky130_fd_pr__pfet_01v8 L=1 W=1.5 nf=1 ad='int((nf+1)/2) * W/nf * 0.29' as='int((nf+2)/2) * W/nf * 0.29'
+ pd='2*int((nf+1)/2) * (W/nf + 0.29)' ps='2*int((nf+2)/2) * (W/nf + 0.29)' nrd='0.29 / W' nrs='0.29 / W'
+ sa=0 sb=0 sd=0 mult=1 m=1
XM6 net6 VDD VDD VDD sky130_fd_pr__pfet_01v8 L=1 W=1.5 nf=1 ad='int((nf+1)/2) * W/nf * 0.29' as='int((nf+2)/2) * W/nf * 0.29'
+ pd='2*int((nf+1)/2) * (W/nf + 0.29)' ps='2*int((nf+2)/2) * (W/nf + 0.29)' nrd='0.29 / W' nrs='0.29 / W'
+ sa=0 sb=0 sd=0 mult=1 m=1
XM10 VDD VDD net6 VDD sky130_fd_pr__pfet_01v8 L=1 W=1.5 nf=1 ad='int((nf+1)/2) * W/nf * 0.29' as='int((nf+2)/2) * W/nf * 0.29'
+ pd='2*int((nf+1)/2) * (W/nf + 0.29)' ps='2*int((nf+2)/2) * (W/nf + 0.29)' nrd='0.29 / W' nrs='0.29 / W'
+ sa=0 sb=0 sd=0 mult=1 m=1
XM26 VDD VDD VDD VDD sky130_fd_pr__pfet_01v8 L=1 W=1.5 nf=1 ad='int((nf+1)/2) * W/nf * 0.29' as='int((nf+2)/2) * W/nf * 0.29'
+ pd='2*int((nf+1)/2) * (W/nf + 0.29)' ps='2*int((nf+2)/2) * (W/nf + 0.29)' nrd='0.29 / W' nrs='0.29 / W'
+ sa=0 sb=0 sd=0 mult=1 m=1
XM27 VDD VDD VDD VDD sky130_fd_pr__pfet_01v8 L=1 W=1.5 nf=1 ad='int((nf+1)/2) * W/nf * 0.29' as='int((nf+2)/2) * W/nf * 0.29'
+ pd='2*int((nf+1)/2) * (W/nf + 0.29)' ps='2*int((nf+2)/2) * (W/nf + 0.29)' nrd='0.29 / W' nrs='0.29 / W'
+ sa=0 sb=0 sd=0 mult=1 m=1
XM50 VDD VDD VDD VDD sky130_fd_pr__pfet_01v8 L=1 W=1.5 nf=1 ad='int((nf+1)/2) * W/nf * 0.29' as='int((nf+2)/2) * W/nf * 0.29'
+ pd='2*int((nf+1)/2) * (W/nf + 0.29)' ps='2*int((nf+2)/2) * (W/nf + 0.29)' nrd='0.29 / W' nrs='0.29 / W'
+ sa=0 sb=0 sd=0 mult=1 m=1
XM51 VDD VDD VDD VDD sky130_fd_pr__pfet_01v8 L=1 W=1.5 nf=1 ad='int((nf+1)/2) * W/nf * 0.29' as='int((nf+2)/2) * W/nf * 0.29'
+ pd='2*int((nf+1)/2) * (W/nf + 0.29)' ps='2*int((nf+2)/2) * (W/nf + 0.29)' nrd='0.29 / W' nrs='0.29 / W'
+ sa=0 sb=0 sd=0 mult=1 m=1
XM52 VDD VDD VDD VDD sky130_fd_pr__pfet_01v8 L=1 W=1.5 nf=1 ad='int((nf+1)/2) * W/nf * 0.29' as='int((nf+2)/2) * W/nf * 0.29'
+ pd='2*int((nf+1)/2) * (W/nf + 0.29)' ps='2*int((nf+2)/2) * (W/nf + 0.29)' nrd='0.29 / W' nrs='0.29 / W'
+ sa=0 sb=0 sd=0 mult=1 m=1
Vout net7 GND 1
VIout net6 net7 0
.save i(viout)
XM12 VDD Vg Vb0 GND sky130_fd_pr__nfet_01v8 L=4 W=16 nf=1 ad='int((nf+1)/2) * W/nf * 0.29' as='int((nf+2)/2) * W/nf * 0.29'
+ pd='2*int((nf+1)/2) * (W/nf + 0.29)' ps='2*int((nf+2)/2) * (W/nf + 0.29)' nrd='0.29 / W' nrs='0.29 / W'
+ sa=0 sb=0 sd=0 mult=1 m=1
XM14 Vb0 Vg VDD GND sky130_fd_pr__nfet_01v8 L=4 W=16 nf=1 ad='int((nf+1)/2) * W/nf * 0.29' as='int((nf+2)/2) * W/nf * 0.29'
+ pd='2*int((nf+1)/2) * (W/nf + 0.29)' ps='2*int((nf+2)/2) * (W/nf + 0.29)' nrd='0.29 / W' nrs='0.29 / W'
+ sa=0 sb=0 sd=0 mult=1 m=1
XMdumb29 Vb1 GND Vb0 GND sky130_fd_pr__nfet_01v8 L=4 W=16 nf=1 ad='int((nf+1)/2) * W/nf * 0.29' as='int((nf+2)/2) * W/nf * 0.29'
+ pd='2*int((nf+1)/2) * (W/nf + 0.29)' ps='2*int((nf+2)/2) * (W/nf + 0.29)' nrd='0.29 / W' nrs='0.29 / W'
+ sa=0 sb=0 sd=0 mult=1 m=1
XM31 VDD Vg Vb1 GND sky130_fd_pr__nfet_01v8 L=4 W=16 nf=1 ad='int((nf+1)/2) * W/nf * 0.29' as='int((nf+2)/2) * W/nf * 0.29'
+ pd='2*int((nf+1)/2) * (W/nf + 0.29)' ps='2*int((nf+2)/2) * (W/nf + 0.29)' nrd='0.29 / W' nrs='0.29 / W'
+ sa=0 sb=0 sd=0 mult=1 m=1
XMdumb32 VDD GND VDD GND sky130_fd_pr__nfet_01v8 L=4 W=16 nf=1 ad='int((nf+1)/2) * W/nf * 0.29' as='int((nf+2)/2) * W/nf * 0.29'
+ pd='2*int((nf+1)/2) * (W/nf + 0.29)' ps='2*int((nf+2)/2) * (W/nf + 0.29)' nrd='0.29 / W' nrs='0.29 / W'
+ sa=0 sb=0 sd=0 mult=1 m=1
XM33 Vb2 Vg VDD GND sky130_fd_pr__nfet_01v8 L=4 W=16 nf=1 ad='int((nf+1)/2) * W/nf * 0.29' as='int((nf+2)/2) * W/nf * 0.29'
+ pd='2*int((nf+1)/2) * (W/nf + 0.29)' ps='2*int((nf+2)/2) * (W/nf + 0.29)' nrd='0.29 / W' nrs='0.29 / W'
+ sa=0 sb=0 sd=0 mult=1 m=1
XMdumb34 Vb3 GND Vb2 GND sky130_fd_pr__nfet_01v8 L=4 W=16 nf=1 ad='int((nf+1)/2) * W/nf * 0.29' as='int((nf+2)/2) * W/nf * 0.29'
+ pd='2*int((nf+1)/2) * (W/nf + 0.29)' ps='2*int((nf+2)/2) * (W/nf + 0.29)' nrd='0.29 / W' nrs='0.29 / W'
+ sa=0 sb=0 sd=0 mult=1 m=1
XM36 VDD Vg Vb3 GND sky130_fd_pr__nfet_01v8 L=4 W=16 nf=1 ad='int((nf+1)/2) * W/nf * 0.29' as='int((nf+2)/2) * W/nf * 0.29'
+ pd='2*int((nf+1)/2) * (W/nf + 0.29)' ps='2*int((nf+2)/2) * (W/nf + 0.29)' nrd='0.29 / W' nrs='0.29 / W'
+ sa=0 sb=0 sd=0 mult=1 m=1
XMdumb37 Vb4 GND VDD GND sky130_fd_pr__nfet_01v8 L=4 W=16 nf=1 ad='int((nf+1)/2) * W/nf * 0.29' as='int((nf+2)/2) * W/nf * 0.29'
+ pd='2*int((nf+1)/2) * (W/nf + 0.29)' ps='2*int((nf+2)/2) * (W/nf + 0.29)' nrd='0.29 / W' nrs='0.29 / W'
+ sa=0 sb=0 sd=0 mult=1 m=1
XM39 VDD Vg Vb4 GND sky130_fd_pr__nfet_01v8 L=4 W=16 nf=1 ad='int((nf+1)/2) * W/nf * 0.29' as='int((nf+2)/2) * W/nf * 0.29'
+ pd='2*int((nf+1)/2) * (W/nf + 0.29)' ps='2*int((nf+2)/2) * (W/nf + 0.29)' nrd='0.29 / W' nrs='0.29 / W'
+ sa=0 sb=0 sd=0 mult=1 m=1
XMdumb40 Vb5 GND VDD GND sky130_fd_pr__nfet_01v8 L=4 W=16 nf=1 ad='int((nf+1)/2) * W/nf * 0.29' as='int((nf+2)/2) * W/nf * 0.29'
+ pd='2*int((nf+1)/2) * (W/nf + 0.29)' ps='2*int((nf+2)/2) * (W/nf + 0.29)' nrd='0.29 / W' nrs='0.29 / W'
+ sa=0 sb=0 sd=0 mult=1 m=1
XM42 net2 Vg Vb5 GND sky130_fd_pr__nfet_01v8 L=4 W=16 nf=1 ad='int((nf+1)/2) * W/nf * 0.29' as='int((nf+2)/2) * W/nf * 0.29'
+ pd='2*int((nf+1)/2) * (W/nf + 0.29)' ps='2*int((nf+2)/2) * (W/nf + 0.29)' nrd='0.29 / W' nrs='0.29 / W'
+ sa=0 sb=0 sd=0 mult=1 m=1
XMdumb43 Vb6 GND net2 GND sky130_fd_pr__nfet_01v8 L=4 W=16 nf=1 ad='int((nf+1)/2) * W/nf * 0.29' as='int((nf+2)/2) * W/nf * 0.29'
+ pd='2*int((nf+1)/2) * (W/nf + 0.29)' ps='2*int((nf+2)/2) * (W/nf + 0.29)' nrd='0.29 / W' nrs='0.29 / W'
+ sa=0 sb=0 sd=0 mult=1 m=1
XM45 net5 Vg Vb6 GND sky130_fd_pr__nfet_01v8 L=4 W=16 nf=1 ad='int((nf+1)/2) * W/nf * 0.29' as='int((nf+2)/2) * W/nf * 0.29'
+ pd='2*int((nf+1)/2) * (W/nf + 0.29)' ps='2*int((nf+2)/2) * (W/nf + 0.29)' nrd='0.29 / W' nrs='0.29 / W'
+ sa=0 sb=0 sd=0 mult=1 m=1
XM46 Vb6 Vg net5 GND sky130_fd_pr__nfet_01v8 L=4 W=16 nf=1 ad='int((nf+1)/2) * W/nf * 0.29' as='int((nf+2)/2) * W/nf * 0.29'
+ pd='2*int((nf+1)/2) * (W/nf + 0.29)' ps='2*int((nf+2)/2) * (W/nf + 0.29)' nrd='0.29 / W' nrs='0.29 / W'
+ sa=0 sb=0 sd=0 mult=1 m=1
XM47 Vb0 Vg Vb1 GND sky130_fd_pr__nfet_01v8 L=4 W=16 nf=1 ad='int((nf+1)/2) * W/nf * 0.29' as='int((nf+2)/2) * W/nf * 0.29'
+ pd='2*int((nf+1)/2) * (W/nf + 0.29)' ps='2*int((nf+2)/2) * (W/nf + 0.29)' nrd='0.29 / W' nrs='0.29 / W'
+ sa=0 sb=0 sd=0 mult=1 m=1
XM48 Vb1 Vg Vb0 GND sky130_fd_pr__nfet_01v8 L=4 W=16 nf=1 ad='int((nf+1)/2) * W/nf * 0.29' as='int((nf+2)/2) * W/nf * 0.29'
+ pd='2*int((nf+1)/2) * (W/nf + 0.29)' ps='2*int((nf+2)/2) * (W/nf + 0.29)' nrd='0.29 / W' nrs='0.29 / W'
+ sa=0 sb=0 sd=0 mult=1 m=1
XM49 Vb2 Vg Vb1 GND sky130_fd_pr__nfet_01v8 L=4 W=16 nf=1 ad='int((nf+1)/2) * W/nf * 0.29' as='int((nf+2)/2) * W/nf * 0.29'
+ pd='2*int((nf+1)/2) * (W/nf + 0.29)' ps='2*int((nf+2)/2) * (W/nf + 0.29)' nrd='0.29 / W' nrs='0.29 / W'
+ sa=0 sb=0 sd=0 mult=1 m=1
XM53 Vb1 Vg Vb2 GND sky130_fd_pr__nfet_01v8 L=4 W=16 nf=1 ad='int((nf+1)/2) * W/nf * 0.29' as='int((nf+2)/2) * W/nf * 0.29'
+ pd='2*int((nf+1)/2) * (W/nf + 0.29)' ps='2*int((nf+2)/2) * (W/nf + 0.29)' nrd='0.29 / W' nrs='0.29 / W'
+ sa=0 sb=0 sd=0 mult=1 m=1
XMdumb54 Vb3 GND Vb1 GND sky130_fd_pr__nfet_01v8 L=4 W=16 nf=1 ad='int((nf+1)/2) * W/nf * 0.29' as='int((nf+2)/2) * W/nf * 0.29'
+ pd='2*int((nf+1)/2) * (W/nf + 0.29)' ps='2*int((nf+2)/2) * (W/nf + 0.29)' nrd='0.29 / W' nrs='0.29 / W'
+ sa=0 sb=0 sd=0 mult=1 m=1
XM55 Vb2 Vg Vb3 GND sky130_fd_pr__nfet_01v8 L=4 W=16 nf=1 ad='int((nf+1)/2) * W/nf * 0.29' as='int((nf+2)/2) * W/nf * 0.29'
+ pd='2*int((nf+1)/2) * (W/nf + 0.29)' ps='2*int((nf+2)/2) * (W/nf + 0.29)' nrd='0.29 / W' nrs='0.29 / W'
+ sa=0 sb=0 sd=0 mult=1 m=1
XM56 Vb3 Vg Vb2 GND sky130_fd_pr__nfet_01v8 L=4 W=16 nf=1 ad='int((nf+1)/2) * W/nf * 0.29' as='int((nf+2)/2) * W/nf * 0.29'
+ pd='2*int((nf+1)/2) * (W/nf + 0.29)' ps='2*int((nf+2)/2) * (W/nf + 0.29)' nrd='0.29 / W' nrs='0.29 / W'
+ sa=0 sb=0 sd=0 mult=1 m=1
XM57 Vb4 Vg Vb3 GND sky130_fd_pr__nfet_01v8 L=4 W=16 nf=1 ad='int((nf+1)/2) * W/nf * 0.29' as='int((nf+2)/2) * W/nf * 0.29'
+ pd='2*int((nf+1)/2) * (W/nf + 0.29)' ps='2*int((nf+2)/2) * (W/nf + 0.29)' nrd='0.29 / W' nrs='0.29 / W'
+ sa=0 sb=0 sd=0 mult=1 m=1
XM58 Vb3 Vg Vb4 GND sky130_fd_pr__nfet_01v8 L=4 W=16 nf=1 ad='int((nf+1)/2) * W/nf * 0.29' as='int((nf+2)/2) * W/nf * 0.29'
+ pd='2*int((nf+1)/2) * (W/nf + 0.29)' ps='2*int((nf+2)/2) * (W/nf + 0.29)' nrd='0.29 / W' nrs='0.29 / W'
+ sa=0 sb=0 sd=0 mult=1 m=1
XMdumb59 Vb5 GND Vb3 GND sky130_fd_pr__nfet_01v8 L=4 W=16 nf=1 ad='int((nf+1)/2) * W/nf * 0.29' as='int((nf+2)/2) * W/nf * 0.29'
+ pd='2*int((nf+1)/2) * (W/nf + 0.29)' ps='2*int((nf+2)/2) * (W/nf + 0.29)' nrd='0.29 / W' nrs='0.29 / W'
+ sa=0 sb=0 sd=0 mult=1 m=1
XM60 Vb4 Vg Vb5 GND sky130_fd_pr__nfet_01v8 L=4 W=16 nf=1 ad='int((nf+1)/2) * W/nf * 0.29' as='int((nf+2)/2) * W/nf * 0.29'
+ pd='2*int((nf+1)/2) * (W/nf + 0.29)' ps='2*int((nf+2)/2) * (W/nf + 0.29)' nrd='0.29 / W' nrs='0.29 / W'
+ sa=0 sb=0 sd=0 mult=1 m=1
XM61 Vb5 Vg Vb4 GND sky130_fd_pr__nfet_01v8 L=4 W=16 nf=1 ad='int((nf+1)/2) * W/nf * 0.29' as='int((nf+2)/2) * W/nf * 0.29'
+ pd='2*int((nf+1)/2) * (W/nf + 0.29)' ps='2*int((nf+2)/2) * (W/nf + 0.29)' nrd='0.29 / W' nrs='0.29 / W'
+ sa=0 sb=0 sd=0 mult=1 m=1
XM62 Vb6 Vg Vb5 GND sky130_fd_pr__nfet_01v8 L=4 W=16 nf=1 ad='int((nf+1)/2) * W/nf * 0.29' as='int((nf+2)/2) * W/nf * 0.29'
+ pd='2*int((nf+1)/2) * (W/nf + 0.29)' ps='2*int((nf+2)/2) * (W/nf + 0.29)' nrd='0.29 / W' nrs='0.29 / W'
+ sa=0 sb=0 sd=0 mult=1 m=1
XM63 Vb5 Vg Vb6 GND sky130_fd_pr__nfet_01v8 L=4 W=16 nf=1 ad='int((nf+1)/2) * W/nf * 0.29' as='int((nf+2)/2) * W/nf * 0.29'
+ pd='2*int((nf+1)/2) * (W/nf + 0.29)' ps='2*int((nf+2)/2) * (W/nf + 0.29)' nrd='0.29 / W' nrs='0.29 / W'
+ sa=0 sb=0 sd=0 mult=1 m=1
XM64 GND Vbn Vb0 GND sky130_fd_pr__nfet_01v8 L=4 W=16 nf=1 ad='int((nf+1)/2) * W/nf * 0.29' as='int((nf+2)/2) * W/nf * 0.29'
+ pd='2*int((nf+1)/2) * (W/nf + 0.29)' ps='2*int((nf+2)/2) * (W/nf + 0.29)' nrd='0.29 / W' nrs='0.29 / W'
+ sa=0 sb=0 sd=0 mult=1 m=1
XMdumb65 Vb0 GND Vb1 GND sky130_fd_pr__nfet_01v8 L=4 W=16 nf=1 ad='int((nf+1)/2) * W/nf * 0.29' as='int((nf+2)/2) * W/nf * 0.29'
+ pd='2*int((nf+1)/2) * (W/nf + 0.29)' ps='2*int((nf+2)/2) * (W/nf + 0.29)' nrd='0.29 / W' nrs='0.29 / W'
+ sa=0 sb=0 sd=0 mult=1 m=1
XM66 Vb1 GND GND GND sky130_fd_pr__nfet_01v8 L=4 W=16 nf=1 ad='int((nf+1)/2) * W/nf * 0.29' as='int((nf+2)/2) * W/nf * 0.29'
+ pd='2*int((nf+1)/2) * (W/nf + 0.29)' ps='2*int((nf+2)/2) * (W/nf + 0.29)' nrd='0.29 / W' nrs='0.29 / W'
+ sa=0 sb=0 sd=0 mult=1 m=1
XM67 GND GND Vb2 GND sky130_fd_pr__nfet_01v8 L=4 W=16 nf=1 ad='int((nf+1)/2) * W/nf * 0.29' as='int((nf+2)/2) * W/nf * 0.29'
+ pd='2*int((nf+1)/2) * (W/nf + 0.29)' ps='2*int((nf+2)/2) * (W/nf + 0.29)' nrd='0.29 / W' nrs='0.29 / W'
+ sa=0 sb=0 sd=0 mult=1 m=1
XMdumb68 Vb2 GND Vb3 GND sky130_fd_pr__nfet_01v8 L=4 W=16 nf=1 ad='int((nf+1)/2) * W/nf * 0.29' as='int((nf+2)/2) * W/nf * 0.29'
+ pd='2*int((nf+1)/2) * (W/nf + 0.29)' ps='2*int((nf+2)/2) * (W/nf + 0.29)' nrd='0.29 / W' nrs='0.29 / W'
+ sa=0 sb=0 sd=0 mult=1 m=1
XM69 Vb3 GND GND GND sky130_fd_pr__nfet_01v8 L=4 W=16 nf=1 ad='int((nf+1)/2) * W/nf * 0.29' as='int((nf+2)/2) * W/nf * 0.29'
+ pd='2*int((nf+1)/2) * (W/nf + 0.29)' ps='2*int((nf+2)/2) * (W/nf + 0.29)' nrd='0.29 / W' nrs='0.29 / W'
+ sa=0 sb=0 sd=0 mult=1 m=1
XM70 GND GND Vb4 GND sky130_fd_pr__nfet_01v8 L=4 W=16 nf=1 ad='int((nf+1)/2) * W/nf * 0.29' as='int((nf+2)/2) * W/nf * 0.29'
+ pd='2*int((nf+1)/2) * (W/nf + 0.29)' ps='2*int((nf+2)/2) * (W/nf + 0.29)' nrd='0.29 / W' nrs='0.29 / W'
+ sa=0 sb=0 sd=0 mult=1 m=1
XMdumb71 Vb4 GND Vb5 GND sky130_fd_pr__nfet_01v8 L=4 W=16 nf=1 ad='int((nf+1)/2) * W/nf * 0.29' as='int((nf+2)/2) * W/nf * 0.29'
+ pd='2*int((nf+1)/2) * (W/nf + 0.29)' ps='2*int((nf+2)/2) * (W/nf + 0.29)' nrd='0.29 / W' nrs='0.29 / W'
+ sa=0 sb=0 sd=0 mult=1 m=1
XM72 Vb5 GND GND GND sky130_fd_pr__nfet_01v8 L=4 W=16 nf=1 ad='int((nf+1)/2) * W/nf * 0.29' as='int((nf+2)/2) * W/nf * 0.29'
+ pd='2*int((nf+1)/2) * (W/nf + 0.29)' ps='2*int((nf+2)/2) * (W/nf + 0.29)' nrd='0.29 / W' nrs='0.29 / W'
+ sa=0 sb=0 sd=0 mult=1 m=1
XM73 GND GND Vb6 GND sky130_fd_pr__nfet_01v8 L=4 W=16 nf=1 ad='int((nf+1)/2) * W/nf * 0.29' as='int((nf+2)/2) * W/nf * 0.29'
+ pd='2*int((nf+1)/2) * (W/nf + 0.29)' ps='2*int((nf+2)/2) * (W/nf + 0.29)' nrd='0.29 / W' nrs='0.29 / W'
+ sa=0 sb=0 sd=0 mult=1 m=1
XMdumb74 GND GND Vb6 GND sky130_fd_pr__nfet_01v8 L=4 W=16 nf=1 ad='int((nf+1)/2) * W/nf * 0.29' as='int((nf+2)/2) * W/nf * 0.29'
+ pd='2*int((nf+1)/2) * (W/nf + 0.29)' ps='2*int((nf+2)/2) * (W/nf + 0.29)' nrd='0.29 / W' nrs='0.29 / W'
+ sa=0 sb=0 sd=0 mult=1 m=1
XMdumb75 GND GND GND GND sky130_fd_pr__nfet_01v8 L=4 W=16 nf=1 ad='int((nf+1)/2) * W/nf * 0.29' as='int((nf+2)/2) * W/nf * 0.29'
+ pd='2*int((nf+1)/2) * (W/nf + 0.29)' ps='2*int((nf+2)/2) * (W/nf + 0.29)' nrd='0.29 / W' nrs='0.29 / W'
+ sa=0 sb=0 sd=0 mult=1 m=1
XMdumb76 Vb0 GND GND GND sky130_fd_pr__nfet_01v8 L=4 W=16 nf=1 ad='int((nf+1)/2) * W/nf * 0.29' as='int((nf+2)/2) * W/nf * 0.29'
+ pd='2*int((nf+1)/2) * (W/nf + 0.29)' ps='2*int((nf+2)/2) * (W/nf + 0.29)' nrd='0.29 / W' nrs='0.29 / W'
+ sa=0 sb=0 sd=0 mult=1 m=1
XMdumb77 GND GND GND GND sky130_fd_pr__nfet_01v8 L=4 W=16 nf=1 ad='int((nf+1)/2) * W/nf * 0.29' as='int((nf+2)/2) * W/nf * 0.29'
+ pd='2*int((nf+1)/2) * (W/nf + 0.29)' ps='2*int((nf+2)/2) * (W/nf + 0.29)' nrd='0.29 / W' nrs='0.29 / W'
+ sa=0 sb=0 sd=0 mult=1 m=1
XMdumb78 Vb1 GND GND GND sky130_fd_pr__nfet_01v8 L=4 W=16 nf=1 ad='int((nf+1)/2) * W/nf * 0.29' as='int((nf+2)/2) * W/nf * 0.29'
+ pd='2*int((nf+1)/2) * (W/nf + 0.29)' ps='2*int((nf+2)/2) * (W/nf + 0.29)' nrd='0.29 / W' nrs='0.29 / W'
+ sa=0 sb=0 sd=0 mult=1 m=1
XMdumb79 GND GND GND GND sky130_fd_pr__nfet_01v8 L=4 W=16 nf=1 ad='int((nf+1)/2) * W/nf * 0.29' as='int((nf+2)/2) * W/nf * 0.29'
+ pd='2*int((nf+1)/2) * (W/nf + 0.29)' ps='2*int((nf+2)/2) * (W/nf + 0.29)' nrd='0.29 / W' nrs='0.29 / W'
+ sa=0 sb=0 sd=0 mult=1 m=1
XMdumb80 GND GND Vb5 GND sky130_fd_pr__nfet_01v8 L=4 W=16 nf=1 ad='int((nf+1)/2) * W/nf * 0.29' as='int((nf+2)/2) * W/nf * 0.29'
+ pd='2*int((nf+1)/2) * (W/nf + 0.29)' ps='2*int((nf+2)/2) * (W/nf + 0.29)' nrd='0.29 / W' nrs='0.29 / W'
+ sa=0 sb=0 sd=0 mult=1 m=1
XMdumb81 GND GND GND GND sky130_fd_pr__nfet_01v8 L=4 W=16 nf=1 ad='int((nf+1)/2) * W/nf * 0.29' as='int((nf+2)/2) * W/nf * 0.29'
+ pd='2*int((nf+1)/2) * (W/nf + 0.29)' ps='2*int((nf+2)/2) * (W/nf + 0.29)' nrd='0.29 / W' nrs='0.29 / W'
+ sa=0 sb=0 sd=0 mult=1 m=1
XM82 GND GND GND GND sky130_fd_pr__nfet_01v8 L=4 W=16 nf=1 ad='int((nf+1)/2) * W/nf * 0.29' as='int((nf+2)/2) * W/nf * 0.29'
+ pd='2*int((nf+1)/2) * (W/nf + 0.29)' ps='2*int((nf+2)/2) * (W/nf + 0.29)' nrd='0.29 / W' nrs='0.29 / W'
+ sa=0 sb=0 sd=0 mult=1 m=1
XMdumb83 Vb6 GND GND GND sky130_fd_pr__nfet_01v8 L=4 W=16 nf=1 ad='int((nf+1)/2) * W/nf * 0.29' as='int((nf+2)/2) * W/nf * 0.29'
+ pd='2*int((nf+1)/2) * (W/nf + 0.29)' ps='2*int((nf+2)/2) * (W/nf + 0.29)' nrd='0.29 / W' nrs='0.29 / W'
+ sa=0 sb=0 sd=0 mult=1 m=1
XMdumb84 GND GND GND GND sky130_fd_pr__nfet_01v8 L=4 W=16 nf=1 ad='int((nf+1)/2) * W/nf * 0.29' as='int((nf+2)/2) * W/nf * 0.29'
+ pd='2*int((nf+1)/2) * (W/nf + 0.29)' ps='2*int((nf+2)/2) * (W/nf + 0.29)' nrd='0.29 / W' nrs='0.29 / W'
+ sa=0 sb=0 sd=0 mult=1 m=1
XMdumb85 GND GND GND GND sky130_fd_pr__nfet_01v8 L=4 W=16 nf=1 ad='int((nf+1)/2) * W/nf * 0.29' as='int((nf+2)/2) * W/nf * 0.29'
+ pd='2*int((nf+1)/2) * (W/nf + 0.29)' ps='2*int((nf+2)/2) * (W/nf + 0.29)' nrd='0.29 / W' nrs='0.29 / W'
+ sa=0 sb=0 sd=0 mult=1 m=1
XMdumb86 GND GND GND GND sky130_fd_pr__nfet_01v8 L=4 W=16 nf=1 ad='int((nf+1)/2) * W/nf * 0.29' as='int((nf+2)/2) * W/nf * 0.29'
+ pd='2*int((nf+1)/2) * (W/nf + 0.29)' ps='2*int((nf+2)/2) * (W/nf + 0.29)' nrd='0.29 / W' nrs='0.29 / W'
+ sa=0 sb=0 sd=0 mult=1 m=1
XMdumb87 GND GND GND GND sky130_fd_pr__nfet_01v8 L=4 W=16 nf=1 ad='int((nf+1)/2) * W/nf * 0.29' as='int((nf+2)/2) * W/nf * 0.29'
+ pd='2*int((nf+1)/2) * (W/nf + 0.29)' ps='2*int((nf+2)/2) * (W/nf + 0.29)' nrd='0.29 / W' nrs='0.29 / W'
+ sa=0 sb=0 sd=0 mult=1 m=1
XMdumb88 GND GND GND GND sky130_fd_pr__nfet_01v8 L=4 W=16 nf=1 ad='int((nf+1)/2) * W/nf * 0.29' as='int((nf+2)/2) * W/nf * 0.29'
+ pd='2*int((nf+1)/2) * (W/nf + 0.29)' ps='2*int((nf+2)/2) * (W/nf + 0.29)' nrd='0.29 / W' nrs='0.29 / W'
+ sa=0 sb=0 sd=0 mult=1 m=1
XMdumb89 GND GND GND GND sky130_fd_pr__nfet_01v8 L=4 W=16 nf=1 ad='int((nf+1)/2) * W/nf * 0.29' as='int((nf+2)/2) * W/nf * 0.29'
+ pd='2*int((nf+1)/2) * (W/nf + 0.29)' ps='2*int((nf+2)/2) * (W/nf + 0.29)' nrd='0.29 / W' nrs='0.29 / W'
+ sa=0 sb=0 sd=0 mult=1 m=1
XMdumb90 GND GND GND GND sky130_fd_pr__nfet_01v8 L=4 W=16 nf=1 ad='int((nf+1)/2) * W/nf * 0.29' as='int((nf+2)/2) * W/nf * 0.29'
+ pd='2*int((nf+1)/2) * (W/nf + 0.29)' ps='2*int((nf+2)/2) * (W/nf + 0.29)' nrd='0.29 / W' nrs='0.29 / W'
+ sa=0 sb=0 sd=0 mult=1 m=1
XMdumb91 GND GND GND GND sky130_fd_pr__nfet_01v8 L=4 W=16 nf=1 ad='int((nf+1)/2) * W/nf * 0.29' as='int((nf+2)/2) * W/nf * 0.29'
+ pd='2*int((nf+1)/2) * (W/nf + 0.29)' ps='2*int((nf+2)/2) * (W/nf + 0.29)' nrd='0.29 / W' nrs='0.29 / W'
+ sa=0 sb=0 sd=0 mult=1 m=1
VIl net3 net1 0
.save i(vil)
**** begin user architecture code

.option wnflag=1
.param MC_SWITCH=0.0
.lib ~/skywater/skywater-pdk/libraries/sky130_fd_pr_ngspice/latest/models/sky130.lib.spice tt


.control
tran 0.000001 10u 0.0001u
save all
plot i(viout) i(vil)
.endc

**** end user architecture code
**.ends
.GLOBAL VDD
.GLOBAL GND
.end
